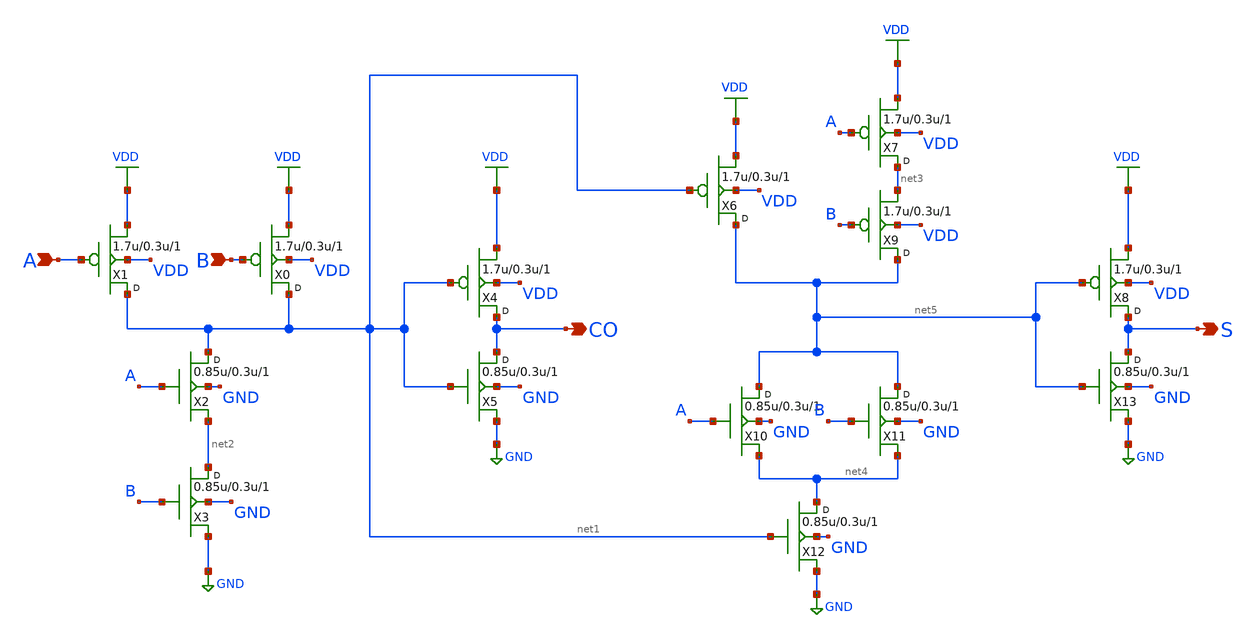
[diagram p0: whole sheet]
** sch_path: lib/12T/xschem/gf180mcu_osu_sc_addh_1.sch
**.subckt gf180mcu_osu_sc_addh_1 A B CO S
*.ipin A
*.ipin B
*.opin CO
*.opin S
X1 net1 A VDD VDD pmos_3p3 w=1.7u l=0.3u m=1
X0 net1 B VDD VDD pmos_3p3 w=1.7u l=0.3u m=1
X2 net1 A net2 GND nmos_3p3 w=0.85u l=0.3u m=1
X3 net2 B GND GND nmos_3p3 w=0.85u l=0.3u m=1
X4 CO net1 VDD VDD pmos_3p3 w=1.7u l=0.3u m=1
X5 CO net1 GND GND nmos_3p3 w=0.85u l=0.3u m=1
X6 net5 net1 VDD VDD pmos_3p3 w=1.7u l=0.3u m=1
X7 net3 A VDD VDD pmos_3p3 w=1.7u l=0.3u m=1
X9 net5 B net3 VDD pmos_3p3 w=1.7u l=0.3u m=1
X10 net5 A net4 GND nmos_3p3 w=0.85u l=0.3u m=1
X11 net5 B net4 GND nmos_3p3 w=0.85u l=0.3u m=1
X12 net4 net1 GND GND nmos_3p3 w=0.85u l=0.3u m=1
X8 S net5 VDD VDD pmos_3p3 w=1.7u l=0.3u m=1
X13 S net5 GND GND nmos_3p3 w=0.85u l=0.3u m=1
**** begin user architecture code


.inc "/import/yukari1/lrburle/OSU_180/char/techfiles/design.hspice"
.lib "/import/yukari1/lrburle/OSU_180/char/techfiles/sm141064.hspice" typical


**** end user architecture code
**.ends
.GLOBAL VDD
.GLOBAL GND
.end
